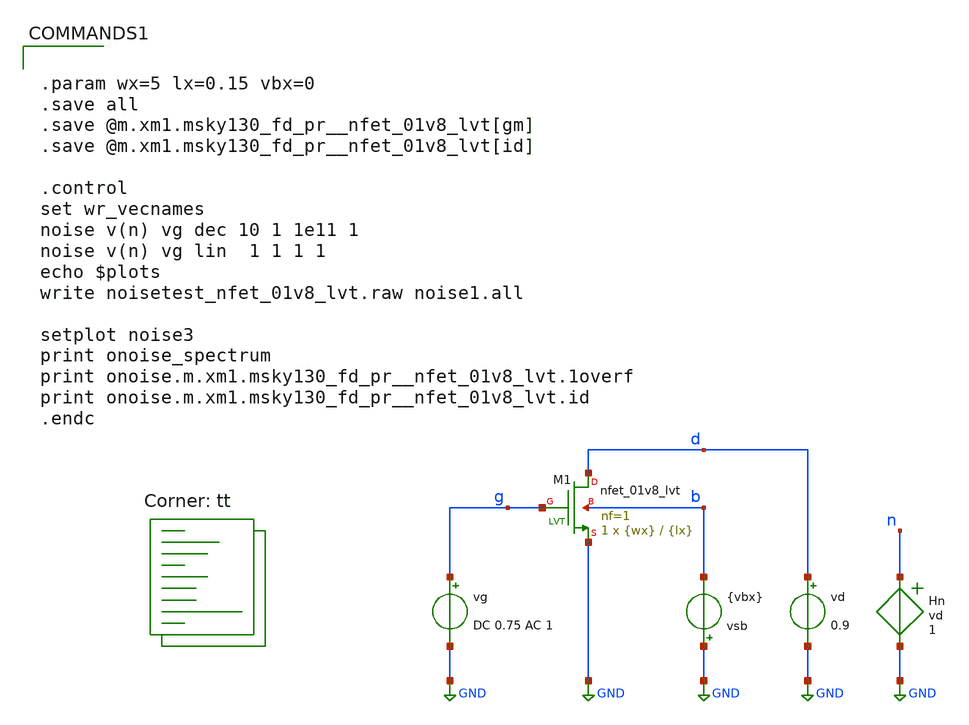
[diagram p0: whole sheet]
** sch_path: starter_files_open_source_tools/sky130/noisetest_nfet_01v8_lvt.sch
**.subckt noisetest_nfet_01v8_lvt
vg g GND DC 0.75 AC 1
vd d GND 0.9
vsb GND b {vbx}
XM1 d g GND b sky130_fd_pr__nfet_01v8_lvt L={lx} W={wx} nf=1 ad='int((nf+1)/2) * W/nf * 0.29' as='int((nf+2)/2) * W/nf * 0.29'
+ pd='2*int((nf+1)/2) * (W/nf + 0.29)' ps='2*int((nf+2)/2) * (W/nf + 0.29)' nrd='0.29 / W' nrs='0.29 / W'
+ sa=0 sb=0 sd=0 mult=1 m=1
Hn n GND vd 1
**** begin user architecture code


.param wx=5 lx=0.15 vbx=0
.save all
.save @m.xm1.msky130_fd_pr__nfet_01v8_lvt[gm]
.save @m.xm1.msky130_fd_pr__nfet_01v8_lvt[id]

.control
set wr_vecnames
noise v(n) vg dec 10 1 1e11 1
noise v(n) vg lin  1 1 1 1
echo $plots
write noisetest_nfet_01v8_lvt.raw noise1.all

setplot noise3
print onoise_spectrum
print onoise.m.xm1.msky130_fd_pr__nfet_01v8_lvt.1overf
print onoise.m.xm1.msky130_fd_pr__nfet_01v8_lvt.id
.endc


.lib $::SKYWATER_MODELS/sky130.lib.spice tt
**** end user architecture code
**.ends
.GLOBAL GND
.end
